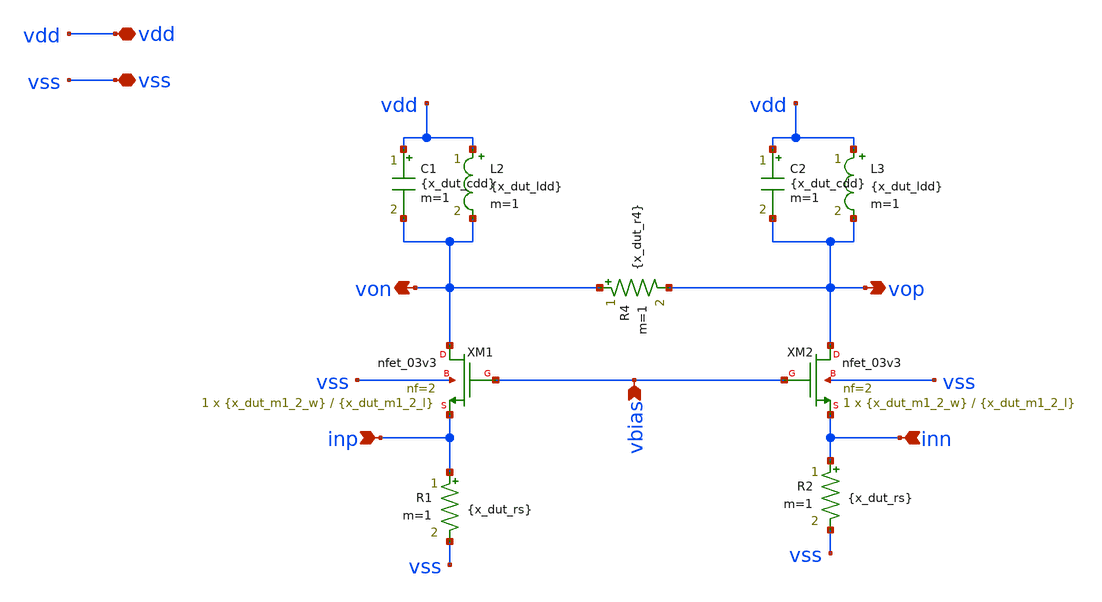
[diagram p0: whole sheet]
** sch_path: examples/tunable-tia/gf180/tia-bpf-1/bpf-tia-1-all-r-c.sch
**.subckt bpf-tia-1-all-r-c vdd vss inp inn von vop vbias
*.iopin vdd
*.iopin vss
*.ipin inp
*.ipin inn
*.opin von
*.opin vop
*.ipin vbias
XM1 von vbias inp vss nfet_03v3 L={x_dut_m1_2_l} W={x_dut_m1_2_w} nf=2 ad='int((nf+1)/2) * W/nf * 0.18u'
+ as='int((nf+2)/2) * W/nf * 0.18u' pd='2*int((nf+1)/2) * (W/nf + 0.18u)' ps='2*int((nf+2)/2) * (W/nf + 0.18u)'
+ nrd='0.18u / W' nrs='0.18u / W' sa=0 sb=0 sd=0 m=1
XM2 vop vbias inn vss nfet_03v3 L={x_dut_m1_2_l} W={x_dut_m1_2_w} nf=2 ad='int((nf+1)/2) * W/nf * 0.18u'
+ as='int((nf+2)/2) * W/nf * 0.18u' pd='2*int((nf+1)/2) * (W/nf + 0.18u)' ps='2*int((nf+2)/2) * (W/nf + 0.18u)'
+ nrd='0.18u / W' nrs='0.18u / W' sa=0 sb=0 sd=0 m=1
R1 inp vss {x_dut_rs} m=1
R2 inn vss {x_dut_rs} m=1
C1 vdd von {x_dut_cdd} m=1
C2 vdd vop {x_dut_cdd} m=1
L2 vdd von {x_dut_ldd} m=1
L3 vdd vop {x_dut_ldd} m=1
R4 von vop {x_dut_r4} m=1
**.ends
.end
